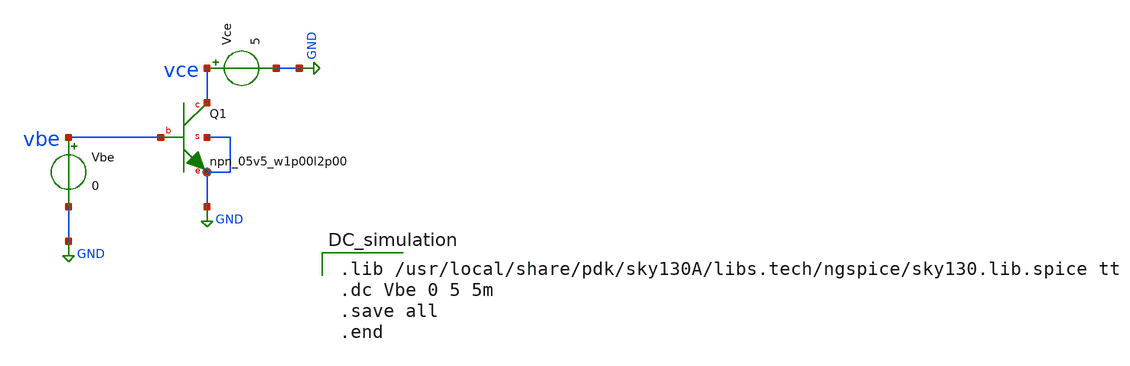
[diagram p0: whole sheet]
** sch_path: xschem/analog_desing/npn_caracterisation.sch
**.subckt npn_caracterisation
XQ1 vce vbe GND GND sky130_fd_pr__npn_05v5_w1p00l2p00
Vbe vbe GND 0
Vce vce GND 5
**** begin user architecture code

.lib /usr/local/share/pdk/sky130A/libs.tech/ngspice/sky130.lib.spice tt
.dc Vbe 0 5 5m
.save all
.end

**** end user architecture code
**.ends
.GLOBAL GND
.end
